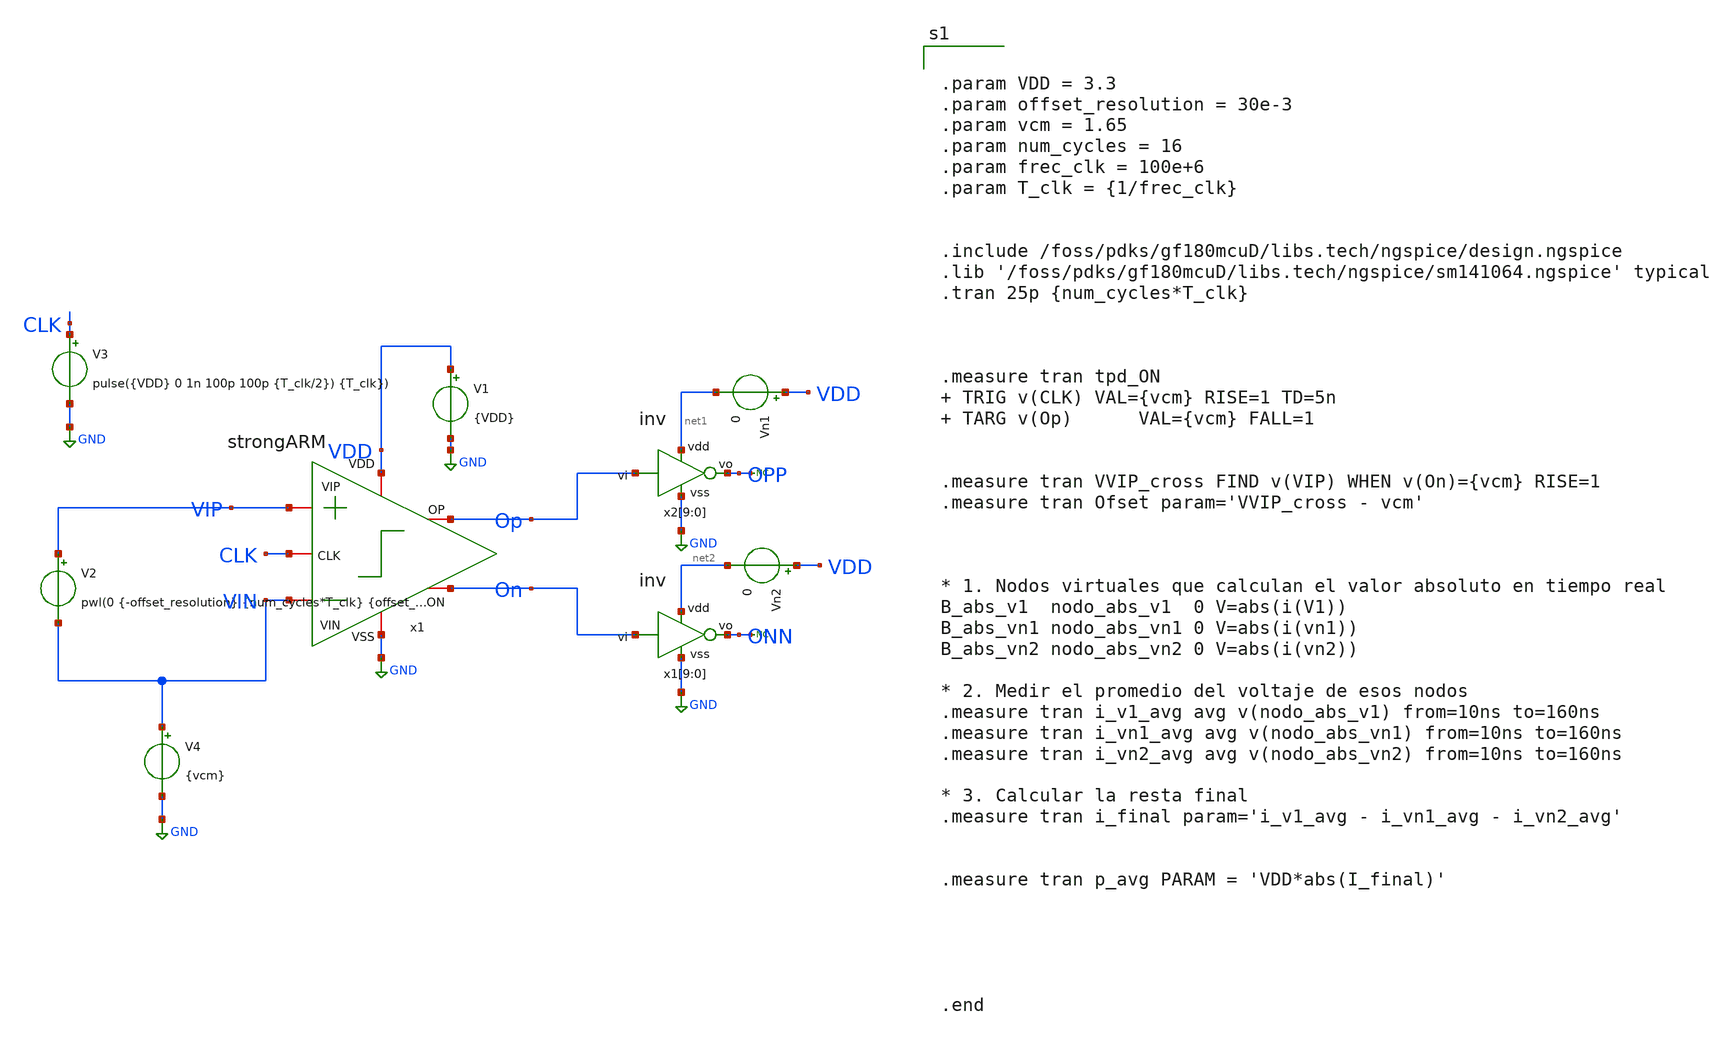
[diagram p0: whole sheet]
** sch_path: designs/sar_adc/comparator/Testbench/tb_strongARM_offset.sch
**.subckt tb_strongARM_offset
V1 VDD GND {VDD}
V2 VIP VIN pwl(0 {-offset_resolution} {num_cycles*T_clk} {offset_resolution})
V3 CLK GND pulse({VDD} 0 1n 100p 100p {T_clk/2}) {T_clk})
V4 VIN GND {vcm}
x1 VDD CLK On Op VIN VIP GND strongARM
x2[9] net1 Op OPP GND inv
x2[8] net1 Op OPP GND inv
x2[7] net1 Op OPP GND inv
x2[6] net1 Op OPP GND inv
x2[5] net1 Op OPP GND inv
x2[4] net1 Op OPP GND inv
x2[3] net1 Op OPP GND inv
x2[2] net1 Op OPP GND inv
x2[1] net1 Op OPP GND inv
x2[0] net1 Op OPP GND inv
x1[9] net2 On ONN GND inv
x1[8] net2 On ONN GND inv
x1[7] net2 On ONN GND inv
x1[6] net2 On ONN GND inv
x1[5] net2 On ONN GND inv
x1[4] net2 On ONN GND inv
x1[3] net2 On ONN GND inv
x1[2] net2 On ONN GND inv
x1[1] net2 On ONN GND inv
x1[0] net2 On ONN GND inv
* noconn ONN
* noconn OPP
Vn1 VDD net1 0
Vn2 VDD net2 0
**** begin user architecture code


.param VDD = 3.3
.param offset_resolution = 30e-3
.param vcm = 1.65
.param num_cycles = 16
.param frec_clk = 100e+6
.param T_clk = {1/frec_clk}


.include /foss/pdks/gf180mcuD/libs.tech/ngspice/design.ngspice
.lib '/foss/pdks/gf180mcuD/libs.tech/ngspice/sm141064.ngspice' typical
.tran 25p {num_cycles*T_clk}



.measure tran tpd_ON  TRIG v(CLK) VAL={vcm} RISE=1 TD=5n  TARG v(Op)      VAL={vcm} FALL=1


.measure tran VVIP_cross FIND v(VIP) WHEN v(On)={vcm} RISE=1
.measure tran Ofset param='VVIP_cross - vcm'



* 1. Nodos virtuales que calculan el valor absoluto en tiempo real
B_abs_v1  nodo_abs_v1  0 V=abs(i(V1))
B_abs_vn1 nodo_abs_vn1 0 V=abs(i(vn1))
B_abs_vn2 nodo_abs_vn2 0 V=abs(i(vn2))

* 2. Medir el promedio del voltaje de esos nodos
.measure tran i_v1_avg avg v(nodo_abs_v1) from=10ns to=160ns
.measure tran i_vn1_avg avg v(nodo_abs_vn1) from=10ns to=160ns
.measure tran i_vn2_avg avg v(nodo_abs_vn2) from=10ns to=160ns

* 3. Calcular la resta final
.measure tran i_final param='i_v1_avg - i_vn1_avg - i_vn2_avg'


.measure tran p_avg PARAM = 'VDD*abs(I_final)'





.end


**** end user architecture code
**.ends
.GLOBAL GND
.end
